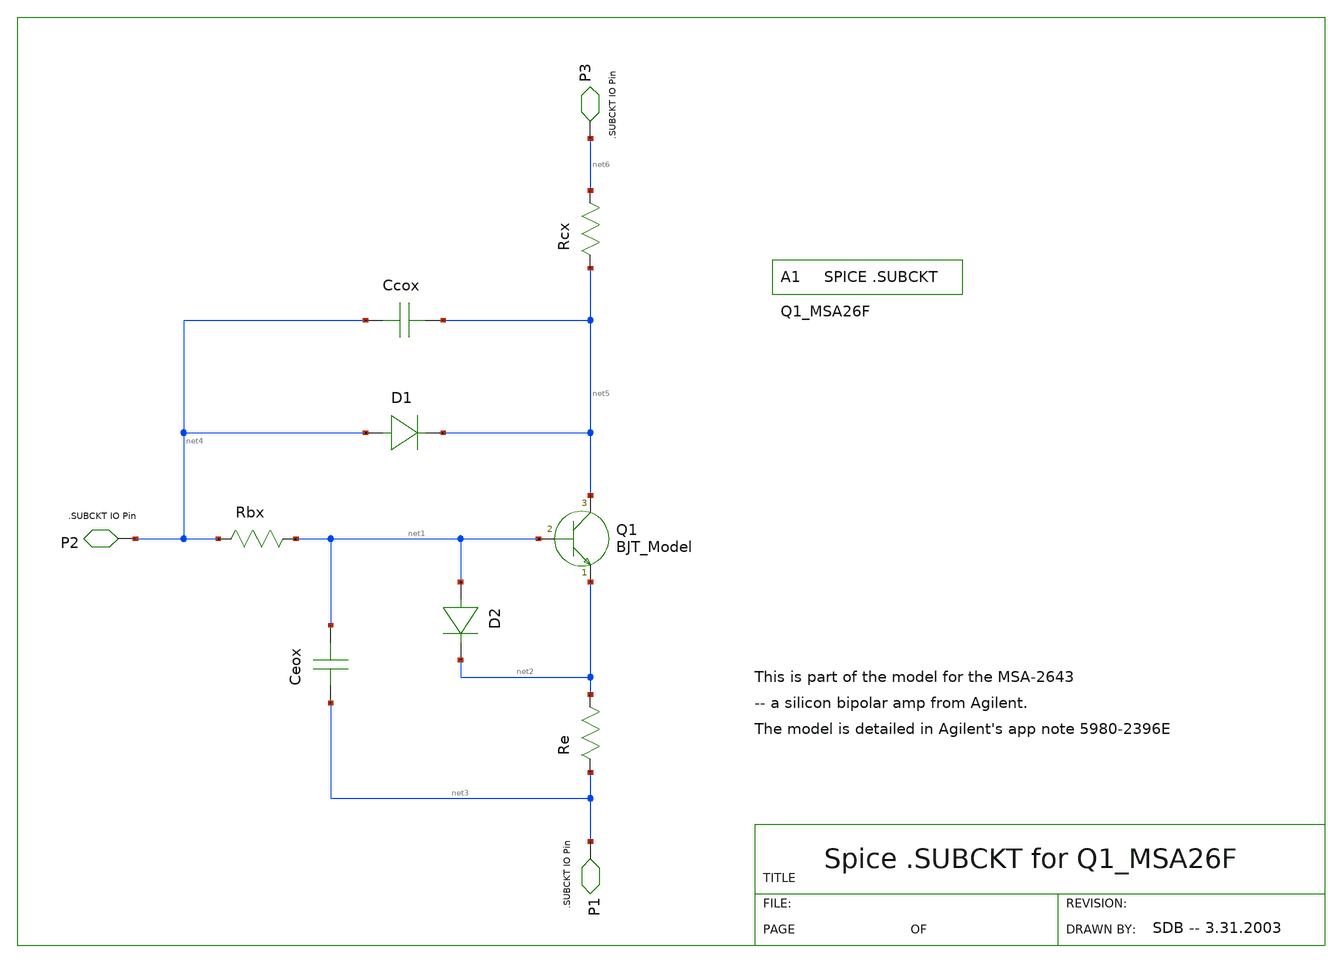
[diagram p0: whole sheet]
** sch_path: xschem-src/xschem_library/gschem_import/Q1.sch
* Copyright (C) 1998-2026 Stefan Frederik Schippers
* This program is free software; you can redistribute it and/or modify
* it under the terms of the GNU General Public License as published by
* the Free Software Foundation; either version 2 of the License, or
* (at your option) any later version.
* This program is distributed in the hope that it will be useful,
* but WITHOUT ANY WARRANTY; without even the implied warranty of
* MERCHANTABILITY or FITNESS FOR A PARTICULAR PURPOSE.  See the
* GNU General Public License for more details.
* You should have received a copy of the GNU General Public License
* along with this program; if not, write to the Free Software
**.subckt Q1
Q1 net5 net1 net2
D1 net4 net5
D2 net1 net2
Ccox net4 net5 1.851e-14F
Ceox net3 net1 6.01e-15F
Rbx net4 net1 3.723
Rcx net5 net6 6.386
Re net3 net2 2.158
P3 net6
P2 net4
P1 net3
A1
**.ends
.end
